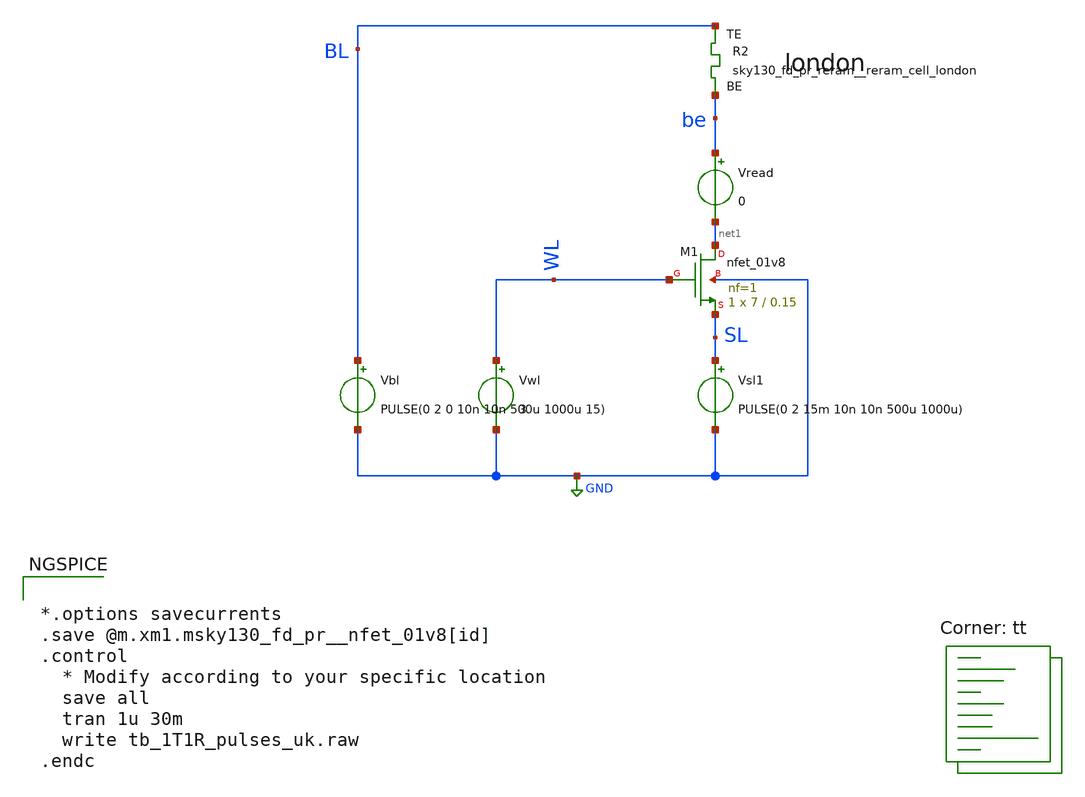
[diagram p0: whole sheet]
** sch_path: memristor_models/rram_london/tb_1T1R_pulses_uk.sch
**.subckt tb_1T1R_pulses_uk
XM1 net1 WL SL GND sky130_fd_pr__nfet_01v8 L=0.15 W=7 nf=1 ad='int((nf+1)/2) * W/nf * 0.29' as='int((nf+2)/2) * W/nf * 0.29'
+ pd='2*int((nf+1)/2) * (W/nf + 0.29)' ps='2*int((nf+2)/2) * (W/nf + 0.29)' nrd='0.29 / W' nrs='0.29 / W'
+ sa=0 sb=0 sd=0 mult=1 m=1
Vwl WL GND 3
Vbl BL GND PULSE(0 2 0 10n 10n 500u 1000u 15)
XR2 BL be sky130_fd_pr_reram__reram_cell_london
Vread be net1 0
Vsl1 SL GND PULSE(0 2 15m 10n 10n 500u 1000u)
**** begin user architecture code


*.options savecurrents
.save @m.xm1.msky130_fd_pr__nfet_01v8[id]
.control
  * Modify according to your specific location
  save all
  tran 1u 30m
  write tb_1T1R_pulses_uk.raw
.endc



.lib $::SKYWATER_MODELS/sky130.lib.spice tt

** opencircuitdesign pdks install
.inc $::SKYWATER_MODELS/sky130_fd_pr_reram__reram_cell_london.spice

**** end user architecture code
**.ends
.GLOBAL GND
.end
